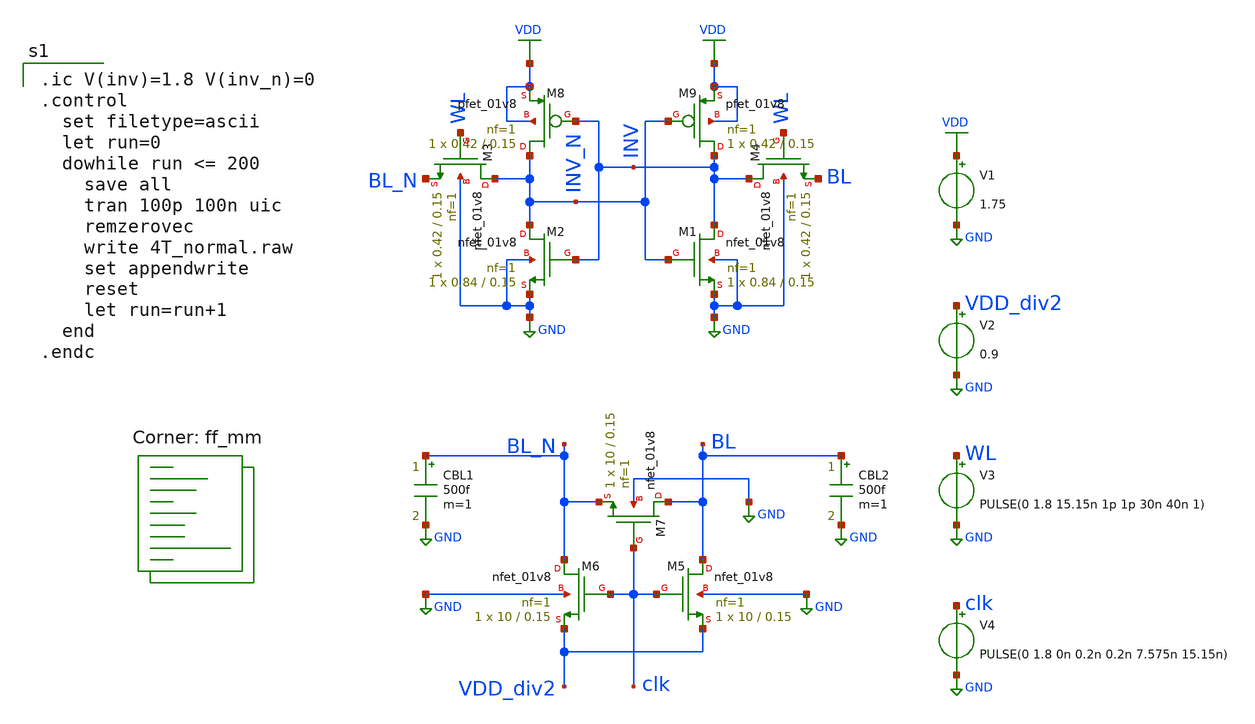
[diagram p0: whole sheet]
** sch_path: analog/schematics/4T_normal.sch
**.subckt 4T_normal
XM1 INV INV_N GND GND sky130_fd_pr__nfet_01v8 L=0.15 W=0.84 nf=1 ad='int((nf+1)/2) * W/nf * 0.29' as='int((nf+2)/2) * W/nf * 0.29'
+ pd='2*int((nf+1)/2) * (W/nf + 0.29)' ps='2*int((nf+2)/2) * (W/nf + 0.29)' nrd='0.29 / W' nrs='0.29 / W'
+ sa=0 sb=0 sd=0 mult=1 m=1
XM3 INV_N WL BL_N GND sky130_fd_pr__nfet_01v8 L=0.15 W=0.42 nf=1 ad='int((nf+1)/2) * W/nf * 0.29' as='int((nf+2)/2) * W/nf * 0.29'
+ pd='2*int((nf+1)/2) * (W/nf + 0.29)' ps='2*int((nf+2)/2) * (W/nf + 0.29)' nrd='0.29 / W' nrs='0.29 / W'
+ sa=0 sb=0 sd=0 mult=1 m=1
XM4 INV WL BL GND sky130_fd_pr__nfet_01v8 L=0.15 W=0.42 nf=1 ad='int((nf+1)/2) * W/nf * 0.29' as='int((nf+2)/2) * W/nf * 0.29'
+ pd='2*int((nf+1)/2) * (W/nf + 0.29)' ps='2*int((nf+2)/2) * (W/nf + 0.29)' nrd='0.29 / W' nrs='0.29 / W'
+ sa=0 sb=0 sd=0 mult=1 m=1
V1 VDD GND 1.75
V2 VDD_div2 GND 0.9
V3 WL GND PULSE(0 1.8 15.15n 1p 1p 30n 40n 1)
V4 clk GND PULSE(0 1.8 0n 0.2n 0.2n 7.575n 15.15n)
XM2 INV_N INV GND GND sky130_fd_pr__nfet_01v8 L=0.15 W=0.84 nf=1 ad='int((nf+1)/2) * W/nf * 0.29' as='int((nf+2)/2) * W/nf * 0.29'
+ pd='2*int((nf+1)/2) * (W/nf + 0.29)' ps='2*int((nf+2)/2) * (W/nf + 0.29)' nrd='0.29 / W' nrs='0.29 / W'
+ sa=0 sb=0 sd=0 mult=1 m=1
XM5 BL clk VDD_div2 GND sky130_fd_pr__nfet_01v8 L=0.15 W=10 nf=1 ad='int((nf+1)/2) * W/nf * 0.29' as='int((nf+2)/2) * W/nf * 0.29'
+ pd='2*int((nf+1)/2) * (W/nf + 0.29)' ps='2*int((nf+2)/2) * (W/nf + 0.29)' nrd='0.29 / W' nrs='0.29 / W'
+ sa=0 sb=0 sd=0 mult=1 m=1
XM6 BL_N clk VDD_div2 GND sky130_fd_pr__nfet_01v8 L=0.15 W=10 nf=1 ad='int((nf+1)/2) * W/nf * 0.29' as='int((nf+2)/2) * W/nf * 0.29'
+ pd='2*int((nf+1)/2) * (W/nf + 0.29)' ps='2*int((nf+2)/2) * (W/nf + 0.29)' nrd='0.29 / W' nrs='0.29 / W'
+ sa=0 sb=0 sd=0 mult=1 m=1
XM7 BL clk BL_N GND sky130_fd_pr__nfet_01v8 L=0.15 W=10 nf=1 ad='int((nf+1)/2) * W/nf * 0.29' as='int((nf+2)/2) * W/nf * 0.29'
+ pd='2*int((nf+1)/2) * (W/nf + 0.29)' ps='2*int((nf+2)/2) * (W/nf + 0.29)' nrd='0.29 / W' nrs='0.29 / W'
+ sa=0 sb=0 sd=0 mult=1 m=1
XM8 INV_N INV VDD VDD sky130_fd_pr__pfet_01v8 L=0.15 W=0.42 nf=1 ad='int((nf+1)/2) * W/nf * 0.29' as='int((nf+2)/2) * W/nf * 0.29'
+ pd='2*int((nf+1)/2) * (W/nf + 0.29)' ps='2*int((nf+2)/2) * (W/nf + 0.29)' nrd='0.29 / W' nrs='0.29 / W'
+ sa=0 sb=0 sd=0 mult=1 m=1
XM9 INV INV_N VDD VDD sky130_fd_pr__pfet_01v8 L=0.15 W=0.42 nf=1 ad='int((nf+1)/2) * W/nf * 0.29' as='int((nf+2)/2) * W/nf * 0.29'
+ pd='2*int((nf+1)/2) * (W/nf + 0.29)' ps='2*int((nf+2)/2) * (W/nf + 0.29)' nrd='0.29 / W' nrs='0.29 / W'
+ sa=0 sb=0 sd=0 mult=1 m=1
CBL1 BL_N GND 500f m=1
CBL2 BL GND 500f m=1
**** begin user architecture code

.ic V(inv)=1.8 V(inv_n)=0
.control
  set filetype=ascii
  let run=0
  dowhile run <= 200
    save all
    tran 100p 100n uic
    remzerovec
    write 4T_normal.raw
    set appendwrite
    reset
    let run=run+1
  end
.endc

.lib $::SKYWATER_MODELS/sky130.lib.spice ff_mm
**** end user architecture code
**.ends
.GLOBAL VDD
.GLOBAL GND
.end
